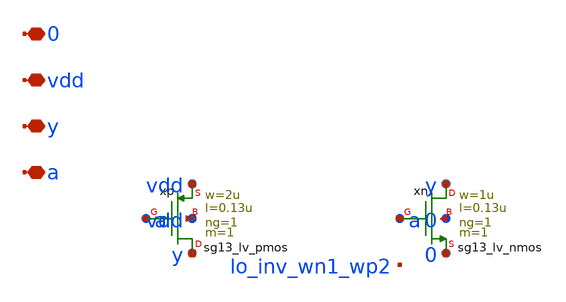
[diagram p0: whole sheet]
** sch_path: analog/lo/sch/lo_inv_1_2.sch
**.subckt lo_inv_1_2 a y vdd 0
*.iopin a
*.iopin y
*.iopin vdd
*.iopin 0
Xxp y a vdd vdd sg13_lv_pmos w=2u l=0.13u ng=1 m=1 mm_ok=1
Xxn y a 0 0 sg13_lv_nmos w=1u l=0.13u ng=1 m=1 mm_ok=1
**.ends
.end
